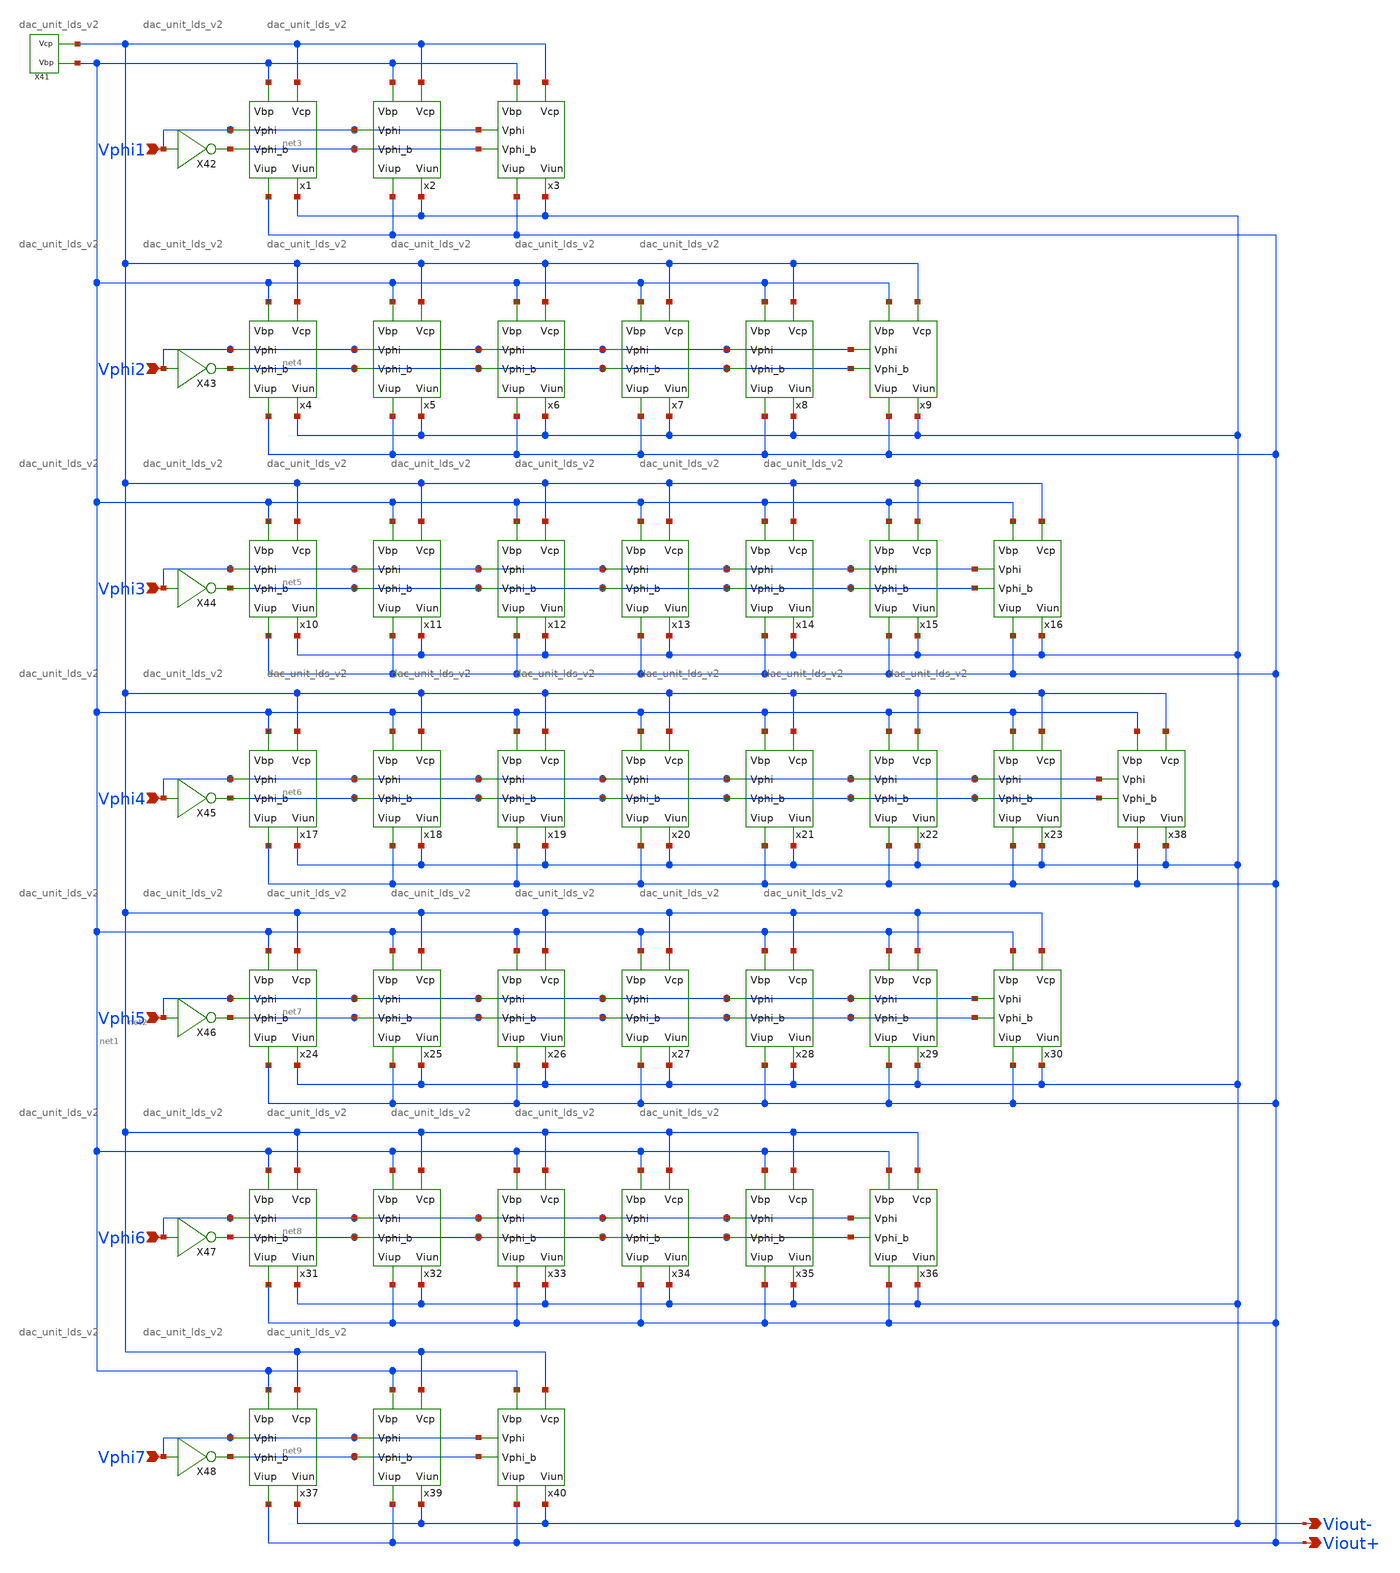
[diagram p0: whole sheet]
** sch_path: simulation/dac_lds.sch
**.subckt dac_lds Vphi1 Vphi2 Vphi3 Vphi4 Vphi5 Vphi6 Vphi7 Viout+ Viout-
*.ipin Vphi1
*.ipin Vphi2
*.ipin Vphi3
*.ipin Vphi4
*.ipin Vphi5
*.ipin Vphi6
*.ipin Vphi7
*.opin Viout+
*.opin Viout-
x1 net1 net2 Viout+ Viout- Vphi1 net3 dac_unit_lds_v2
x2 net1 net2 Viout+ Viout- Vphi1 net3 dac_unit_lds_v2
x3 net1 net2 Viout+ Viout- Vphi1 net3 dac_unit_lds_v2
x4 net1 net2 Viout+ Viout- Vphi2 net4 dac_unit_lds_v2
x5 net1 net2 Viout+ Viout- Vphi2 net4 dac_unit_lds_v2
x6 net1 net2 Viout+ Viout- Vphi2 net4 dac_unit_lds_v2
x7 net1 net2 Viout+ Viout- Vphi2 net4 dac_unit_lds_v2
x8 net1 net2 Viout+ Viout- Vphi2 net4 dac_unit_lds_v2
x9 net1 net2 Viout+ Viout- Vphi2 net4 dac_unit_lds_v2
x10 net1 net2 Viout+ Viout- Vphi3 net5 dac_unit_lds_v2
x11 net1 net2 Viout+ Viout- Vphi3 net5 dac_unit_lds_v2
x12 net1 net2 Viout+ Viout- Vphi3 net5 dac_unit_lds_v2
x13 net1 net2 Viout+ Viout- Vphi3 net5 dac_unit_lds_v2
x14 net1 net2 Viout+ Viout- Vphi3 net5 dac_unit_lds_v2
x15 net1 net2 Viout+ Viout- Vphi3 net5 dac_unit_lds_v2
x16 net1 net2 Viout+ Viout- Vphi3 net5 dac_unit_lds_v2
x17 net1 net2 Viout+ Viout- Vphi4 net6 dac_unit_lds_v2
x18 net1 net2 Viout+ Viout- Vphi4 net6 dac_unit_lds_v2
x19 net1 net2 Viout+ Viout- Vphi4 net6 dac_unit_lds_v2
x20 net1 net2 Viout+ Viout- Vphi4 net6 dac_unit_lds_v2
x21 net1 net2 Viout+ Viout- Vphi4 net6 dac_unit_lds_v2
x22 net1 net2 Viout+ Viout- Vphi4 net6 dac_unit_lds_v2
x23 net1 net2 Viout+ Viout- Vphi4 net6 dac_unit_lds_v2
x24 net1 net2 Viout+ Viout- Vphi5 net7 dac_unit_lds_v2
x25 net1 net2 Viout+ Viout- Vphi5 net7 dac_unit_lds_v2
x26 net1 net2 Viout+ Viout- Vphi5 net7 dac_unit_lds_v2
x27 net1 net2 Viout+ Viout- Vphi5 net7 dac_unit_lds_v2
x28 net1 net2 Viout+ Viout- Vphi5 net7 dac_unit_lds_v2
x29 net1 net2 Viout+ Viout- Vphi5 net7 dac_unit_lds_v2
x30 net1 net2 Viout+ Viout- Vphi5 net7 dac_unit_lds_v2
x31 net1 net2 Viout+ Viout- Vphi6 net8 dac_unit_lds_v2
x32 net1 net2 Viout+ Viout- Vphi6 net8 dac_unit_lds_v2
x33 net1 net2 Viout+ Viout- Vphi6 net8 dac_unit_lds_v2
x34 net1 net2 Viout+ Viout- Vphi6 net8 dac_unit_lds_v2
x35 net1 net2 Viout+ Viout- Vphi6 net8 dac_unit_lds_v2
x36 net1 net2 Viout+ Viout- Vphi6 net8 dac_unit_lds_v2
x38 net1 net2 Viout+ Viout- Vphi4 net6 dac_unit_lds_v2
x37 net1 net2 Viout+ Viout- Vphi7 net9 dac_unit_lds_v2
x39 net1 net2 Viout+ Viout- Vphi7 net9 dac_unit_lds_v2
x40 net1 net2 Viout+ Viout- Vphi7 net9 dac_unit_lds_v2
X41 net2 net1 v_gen_lds
X42 Vphi1 net3 inverter
X43 Vphi2 net4 inverter
X44 Vphi3 net5 inverter
X45 Vphi4 net6 inverter
X46 Vphi5 net7 inverter
X47 Vphi6 net8 inverter
X48 Vphi7 net9 inverter
**.ends

* expanding   symbol:  ./dac/dac_unit_lds_v2.sym # of pins=6
** sym_path: simulation/dac/dac_unit_lds_v2.sym
** sch_path: simulation/dac/dac_unit_lds_v2.sch
.subckt dac_unit_lds_v2 Vbp Vcp Viup Viun Vphi Vphi_b
*.ipin Vphi
*.ipin Vbp
*.ipin Vcp
*.opin Viun
*.opin Viup
*.ipin Vphi_b
XM1 net1 Vbp VDD VDD sky130_fd_pr__pfet_01v8 L=0.5 W=6 nf=1 ad='int((nf+1)/2) * W/nf * 0.29' as='int((nf+2)/2) * W/nf * 0.29'
+ pd='2*int((nf+1)/2) * (W/nf + 0.29)' ps='2*int((nf+2)/2) * (W/nf + 0.29)' nrd='0.29 / W' nrs='0.29 / W'
+ sa=0 sb=0 sd=0 mult=1 m=1
XM2 net2 Vcp net1 VDD sky130_fd_pr__pfet_01v8 L=0.5 W=6 nf=1 ad='int((nf+1)/2) * W/nf * 0.29' as='int((nf+2)/2) * W/nf * 0.29'
+ pd='2*int((nf+1)/2) * (W/nf + 0.29)' ps='2*int((nf+2)/2) * (W/nf + 0.29)' nrd='0.29 / W' nrs='0.29 / W'
+ sa=0 sb=0 sd=0 mult=1 m=1
XM3 Viun Vphi net2 VDD sky130_fd_pr__pfet_01v8 L=0.5 W=6 nf=1 ad='int((nf+1)/2) * W/nf * 0.29' as='int((nf+2)/2) * W/nf * 0.29'
+ pd='2*int((nf+1)/2) * (W/nf + 0.29)' ps='2*int((nf+2)/2) * (W/nf + 0.29)' nrd='0.29 / W' nrs='0.29 / W'
+ sa=0 sb=0 sd=0 mult=1 m=1
XM4 Viup Vphi_b net2 VDD sky130_fd_pr__pfet_01v8 L=0.5 W=6 nf=1 ad='int((nf+1)/2) * W/nf * 0.29' as='int((nf+2)/2) * W/nf * 0.29'
+ pd='2*int((nf+1)/2) * (W/nf + 0.29)' ps='2*int((nf+2)/2) * (W/nf + 0.29)' nrd='0.29 / W' nrs='0.29 / W'
+ sa=0 sb=0 sd=0 mult=1 m=1
XM5 net3 Vbp VDD VDD sky130_fd_pr__pfet_01v8 L=0.5 W=6 nf=1 ad='int((nf+1)/2) * W/nf * 0.29' as='int((nf+2)/2) * W/nf * 0.29'
+ pd='2*int((nf+1)/2) * (W/nf + 0.29)' ps='2*int((nf+2)/2) * (W/nf + 0.29)' nrd='0.29 / W' nrs='0.29 / W'
+ sa=0 sb=0 sd=0 mult=1 m=1
XM6 net4 Vcp net3 VDD sky130_fd_pr__pfet_01v8 L=0.5 W=6 nf=1 ad='int((nf+1)/2) * W/nf * 0.29' as='int((nf+2)/2) * W/nf * 0.29'
+ pd='2*int((nf+1)/2) * (W/nf + 0.29)' ps='2*int((nf+2)/2) * (W/nf + 0.29)' nrd='0.29 / W' nrs='0.29 / W'
+ sa=0 sb=0 sd=0 mult=1 m=1
XM7 Viun Vphi net4 VDD sky130_fd_pr__pfet_01v8 L=0.5 W=6 nf=1 ad='int((nf+1)/2) * W/nf * 0.29' as='int((nf+2)/2) * W/nf * 0.29'
+ pd='2*int((nf+1)/2) * (W/nf + 0.29)' ps='2*int((nf+2)/2) * (W/nf + 0.29)' nrd='0.29 / W' nrs='0.29 / W'
+ sa=0 sb=0 sd=0 mult=1 m=1
XM8 Viup Vphi_b net4 VDD sky130_fd_pr__pfet_01v8 L=0.5 W=6 nf=1 ad='int((nf+1)/2) * W/nf * 0.29' as='int((nf+2)/2) * W/nf * 0.29'
+ pd='2*int((nf+1)/2) * (W/nf + 0.29)' ps='2*int((nf+2)/2) * (W/nf + 0.29)' nrd='0.29 / W' nrs='0.29 / W'
+ sa=0 sb=0 sd=0 mult=1 m=1
XM9 VDD VDD net1 VDD sky130_fd_pr__pfet_01v8 L=0.5 W=6 nf=1 ad='int((nf+1)/2) * W/nf * 0.29' as='int((nf+2)/2) * W/nf * 0.29'
+ pd='2*int((nf+1)/2) * (W/nf + 0.29)' ps='2*int((nf+2)/2) * (W/nf + 0.29)' nrd='0.29 / W' nrs='0.29 / W'
+ sa=0 sb=0 sd=0 mult=1 m=1
XM10 net1 VDD VDD VDD sky130_fd_pr__pfet_01v8 L=0.5 W=6 nf=1 ad='int((nf+1)/2) * W/nf * 0.29' as='int((nf+2)/2) * W/nf * 0.29'
+ pd='2*int((nf+1)/2) * (W/nf + 0.29)' ps='2*int((nf+2)/2) * (W/nf + 0.29)' nrd='0.29 / W' nrs='0.29 / W'
+ sa=0 sb=0 sd=0 mult=1 m=1
XM11 VDD VDD net3 VDD sky130_fd_pr__pfet_01v8 L=0.5 W=6 nf=1 ad='int((nf+1)/2) * W/nf * 0.29' as='int((nf+2)/2) * W/nf * 0.29'
+ pd='2*int((nf+1)/2) * (W/nf + 0.29)' ps='2*int((nf+2)/2) * (W/nf + 0.29)' nrd='0.29 / W' nrs='0.29 / W'
+ sa=0 sb=0 sd=0 mult=1 m=1
XM12 net3 VDD VDD VDD sky130_fd_pr__pfet_01v8 L=0.5 W=6 nf=1 ad='int((nf+1)/2) * W/nf * 0.29' as='int((nf+2)/2) * W/nf * 0.29'
+ pd='2*int((nf+1)/2) * (W/nf + 0.29)' ps='2*int((nf+2)/2) * (W/nf + 0.29)' nrd='0.29 / W' nrs='0.29 / W'
+ sa=0 sb=0 sd=0 mult=1 m=1
.ends


* expanding   symbol:  ./dac/v_gen_lds.sym # of pins=2
** sym_path: simulation/dac/v_gen_lds.sym
** sch_path: simulation/dac/v_gen_lds.sch
.subckt v_gen_lds Vcp Vbp
*.opin Vcp
*.opin Vbp
XM25 net1 Vcp Vcp VDD sky130_fd_pr__pfet_01v8 L=0.5 W=12 nf=1 ad='int((nf+1)/2) * W/nf * 0.29' as='int((nf+2)/2) * W/nf * 0.29'
+ pd='2*int((nf+1)/2) * (W/nf + 0.29)' ps='2*int((nf+2)/2) * (W/nf + 0.29)' nrd='0.29 / W' nrs='0.29 / W'
+ sa=0 sb=0 sd=0 mult=1 m=1
XM26 Vcp net3 GND GND sky130_fd_pr__nfet_01v8 L=0.5 W=12 nf=1 ad='int((nf+1)/2) * W/nf * 0.29' as='int((nf+2)/2) * W/nf * 0.29'
+ pd='2*int((nf+1)/2) * (W/nf + 0.29)' ps='2*int((nf+2)/2) * (W/nf + 0.29)' nrd='0.29 / W' nrs='0.29 / W'
+ sa=0 sb=0 sd=0 mult=1 m=1
XM27 net2 net2 net1 VDD sky130_fd_pr__pfet_01v8 L=0.5 W=12 nf=1 ad='int((nf+1)/2) * W/nf * 0.29' as='int((nf+2)/2) * W/nf * 0.29'
+ pd='2*int((nf+1)/2) * (W/nf + 0.29)' ps='2*int((nf+2)/2) * (W/nf + 0.29)' nrd='0.29 / W' nrs='0.29 / W'
+ sa=0 sb=0 sd=0 mult=1 m=1
XM28 GND net3 net4 GND sky130_fd_pr__nfet_01v8 L=0.5 W=12 nf=1 ad='int((nf+1)/2) * W/nf * 0.29' as='int((nf+2)/2) * W/nf * 0.29'
+ pd='2*int((nf+1)/2) * (W/nf + 0.29)' ps='2*int((nf+2)/2) * (W/nf + 0.29)' nrd='0.29 / W' nrs='0.29 / W'
+ sa=0 sb=0 sd=0 mult=1 m=1
XM41 net1 net2 net2 VDD sky130_fd_pr__pfet_01v8 L=0.5 W=12 nf=1 ad='int((nf+1)/2) * W/nf * 0.29' as='int((nf+2)/2) * W/nf * 0.29'
+ pd='2*int((nf+1)/2) * (W/nf + 0.29)' ps='2*int((nf+2)/2) * (W/nf + 0.29)' nrd='0.29 / W' nrs='0.29 / W'
+ sa=0 sb=0 sd=0 mult=1 m=1
XM42 net4 net3 net5 GND sky130_fd_pr__nfet_01v8 L=0.5 W=12 nf=1 ad='int((nf+1)/2) * W/nf * 0.29' as='int((nf+2)/2) * W/nf * 0.29'
+ pd='2*int((nf+1)/2) * (W/nf + 0.29)' ps='2*int((nf+2)/2) * (W/nf + 0.29)' nrd='0.29 / W' nrs='0.29 / W'
+ sa=0 sb=0 sd=0 mult=1 m=1
XM43 net2 net2 net1 VDD sky130_fd_pr__pfet_01v8 L=0.5 W=12 nf=1 ad='int((nf+1)/2) * W/nf * 0.29' as='int((nf+2)/2) * W/nf * 0.29'
+ pd='2*int((nf+1)/2) * (W/nf + 0.29)' ps='2*int((nf+2)/2) * (W/nf + 0.29)' nrd='0.29 / W' nrs='0.29 / W'
+ sa=0 sb=0 sd=0 mult=1 m=1
XM44 net5 net3 net6 GND sky130_fd_pr__nfet_01v8 L=0.5 W=12 nf=1 ad='int((nf+1)/2) * W/nf * 0.29' as='int((nf+2)/2) * W/nf * 0.29'
+ pd='2*int((nf+1)/2) * (W/nf + 0.29)' ps='2*int((nf+2)/2) * (W/nf + 0.29)' nrd='0.29 / W' nrs='0.29 / W'
+ sa=0 sb=0 sd=0 mult=1 m=1
XM45 net1 net2 net2 VDD sky130_fd_pr__pfet_01v8 L=0.5 W=12 nf=1 ad='int((nf+1)/2) * W/nf * 0.29' as='int((nf+2)/2) * W/nf * 0.29'
+ pd='2*int((nf+1)/2) * (W/nf + 0.29)' ps='2*int((nf+2)/2) * (W/nf + 0.29)' nrd='0.29 / W' nrs='0.29 / W'
+ sa=0 sb=0 sd=0 mult=1 m=1
XM46 net6 net3 net7 GND sky130_fd_pr__nfet_01v8 L=0.5 W=12 nf=1 ad='int((nf+1)/2) * W/nf * 0.29' as='int((nf+2)/2) * W/nf * 0.29'
+ pd='2*int((nf+1)/2) * (W/nf + 0.29)' ps='2*int((nf+2)/2) * (W/nf + 0.29)' nrd='0.29 / W' nrs='0.29 / W'
+ sa=0 sb=0 sd=0 mult=1 m=1
XM47 VDD net2 net1 VDD sky130_fd_pr__pfet_01v8 L=0.5 W=12 nf=1 ad='int((nf+1)/2) * W/nf * 0.29' as='int((nf+2)/2) * W/nf * 0.29'
+ pd='2*int((nf+1)/2) * (W/nf + 0.29)' ps='2*int((nf+2)/2) * (W/nf + 0.29)' nrd='0.29 / W' nrs='0.29 / W'
+ sa=0 sb=0 sd=0 mult=1 m=1
XM48 net7 net3 net2 GND sky130_fd_pr__nfet_01v8 L=0.5 W=12 nf=1 ad='int((nf+1)/2) * W/nf * 0.29' as='int((nf+2)/2) * W/nf * 0.29'
+ pd='2*int((nf+1)/2) * (W/nf + 0.29)' ps='2*int((nf+2)/2) * (W/nf + 0.29)' nrd='0.29 / W' nrs='0.29 / W'
+ sa=0 sb=0 sd=0 mult=1 m=1
XM54 VDD Vbp Vbp VDD sky130_fd_pr__pfet_01v8 L=0.5 W=12 nf=1 ad='int((nf+1)/2) * W/nf * 0.29' as='int((nf+2)/2) * W/nf * 0.29'
+ pd='2*int((nf+1)/2) * (W/nf + 0.29)' ps='2*int((nf+2)/2) * (W/nf + 0.29)' nrd='0.29 / W' nrs='0.29 / W'
+ sa=0 sb=0 sd=0 mult=1 m=1
XM1 Vbp net3 GND GND sky130_fd_pr__nfet_01v8 L=0.5 W=12 nf=1 ad='int((nf+1)/2) * W/nf * 0.29' as='int((nf+2)/2) * W/nf * 0.29'
+ pd='2*int((nf+1)/2) * (W/nf + 0.29)' ps='2*int((nf+2)/2) * (W/nf + 0.29)' nrd='0.29 / W' nrs='0.29 / W'
+ sa=0 sb=0 sd=0 mult=1 m=1
XM2 net3 net3 GND GND sky130_fd_pr__nfet_01v8 L=0.5 W=12 nf=1 ad='int((nf+1)/2) * W/nf * 0.29' as='int((nf+2)/2) * W/nf * 0.29'
+ pd='2*int((nf+1)/2) * (W/nf + 0.29)' ps='2*int((nf+2)/2) * (W/nf + 0.29)' nrd='0.29 / W' nrs='0.29 / W'
+ sa=0 sb=0 sd=0 mult=1 m=1
XM3 Vcp VDD VDD VDD sky130_fd_pr__pfet_01v8 L=0.5 W=12 nf=1 ad='int((nf+1)/2) * W/nf * 0.29' as='int((nf+2)/2) * W/nf * 0.29'
+ pd='2*int((nf+1)/2) * (W/nf + 0.29)' ps='2*int((nf+2)/2) * (W/nf + 0.29)' nrd='0.29 / W' nrs='0.29 / W'
+ sa=0 sb=0 sd=0 mult=1 m=1
XM16 net8 net13 net13 VDD sky130_fd_pr__pfet_01v8 L=0.5 W=12 nf=1 ad='int((nf+1)/2) * W/nf * 0.29' as='int((nf+2)/2) * W/nf * 0.29'
+ pd='2*int((nf+1)/2) * (W/nf + 0.29)' ps='2*int((nf+2)/2) * (W/nf + 0.29)' nrd='0.29 / W' nrs='0.29 / W'
+ sa=0 sb=0 sd=0 mult=1 m=1
XM17 net13 net3 GND GND sky130_fd_pr__nfet_01v8 L=0.5 W=12 nf=1 ad='int((nf+1)/2) * W/nf * 0.29' as='int((nf+2)/2) * W/nf * 0.29'
+ pd='2*int((nf+1)/2) * (W/nf + 0.29)' ps='2*int((nf+2)/2) * (W/nf + 0.29)' nrd='0.29 / W' nrs='0.29 / W'
+ sa=0 sb=0 sd=0 mult=1 m=1
XM18 net2 net2 net8 VDD sky130_fd_pr__pfet_01v8 L=0.5 W=12 nf=1 ad='int((nf+1)/2) * W/nf * 0.29' as='int((nf+2)/2) * W/nf * 0.29'
+ pd='2*int((nf+1)/2) * (W/nf + 0.29)' ps='2*int((nf+2)/2) * (W/nf + 0.29)' nrd='0.29 / W' nrs='0.29 / W'
+ sa=0 sb=0 sd=0 mult=1 m=1
XM19 GND net3 net9 GND sky130_fd_pr__nfet_01v8 L=0.5 W=12 nf=1 ad='int((nf+1)/2) * W/nf * 0.29' as='int((nf+2)/2) * W/nf * 0.29'
+ pd='2*int((nf+1)/2) * (W/nf + 0.29)' ps='2*int((nf+2)/2) * (W/nf + 0.29)' nrd='0.29 / W' nrs='0.29 / W'
+ sa=0 sb=0 sd=0 mult=1 m=1
XM20 net8 net2 net2 VDD sky130_fd_pr__pfet_01v8 L=0.5 W=12 nf=1 ad='int((nf+1)/2) * W/nf * 0.29' as='int((nf+2)/2) * W/nf * 0.29'
+ pd='2*int((nf+1)/2) * (W/nf + 0.29)' ps='2*int((nf+2)/2) * (W/nf + 0.29)' nrd='0.29 / W' nrs='0.29 / W'
+ sa=0 sb=0 sd=0 mult=1 m=1
XM21 net9 net3 net10 GND sky130_fd_pr__nfet_01v8 L=0.5 W=12 nf=1 ad='int((nf+1)/2) * W/nf * 0.29' as='int((nf+2)/2) * W/nf * 0.29'
+ pd='2*int((nf+1)/2) * (W/nf + 0.29)' ps='2*int((nf+2)/2) * (W/nf + 0.29)' nrd='0.29 / W' nrs='0.29 / W'
+ sa=0 sb=0 sd=0 mult=1 m=1
XM22 net2 net2 net8 VDD sky130_fd_pr__pfet_01v8 L=0.5 W=12 nf=1 ad='int((nf+1)/2) * W/nf * 0.29' as='int((nf+2)/2) * W/nf * 0.29'
+ pd='2*int((nf+1)/2) * (W/nf + 0.29)' ps='2*int((nf+2)/2) * (W/nf + 0.29)' nrd='0.29 / W' nrs='0.29 / W'
+ sa=0 sb=0 sd=0 mult=1 m=1
XM23 net10 net3 net11 GND sky130_fd_pr__nfet_01v8 L=0.5 W=12 nf=1 ad='int((nf+1)/2) * W/nf * 0.29' as='int((nf+2)/2) * W/nf * 0.29'
+ pd='2*int((nf+1)/2) * (W/nf + 0.29)' ps='2*int((nf+2)/2) * (W/nf + 0.29)' nrd='0.29 / W' nrs='0.29 / W'
+ sa=0 sb=0 sd=0 mult=1 m=1
XM24 net8 net2 net2 VDD sky130_fd_pr__pfet_01v8 L=0.5 W=12 nf=1 ad='int((nf+1)/2) * W/nf * 0.29' as='int((nf+2)/2) * W/nf * 0.29'
+ pd='2*int((nf+1)/2) * (W/nf + 0.29)' ps='2*int((nf+2)/2) * (W/nf + 0.29)' nrd='0.29 / W' nrs='0.29 / W'
+ sa=0 sb=0 sd=0 mult=1 m=1
XM49 net11 net3 net12 GND sky130_fd_pr__nfet_01v8 L=0.5 W=12 nf=1 ad='int((nf+1)/2) * W/nf * 0.29' as='int((nf+2)/2) * W/nf * 0.29'
+ pd='2*int((nf+1)/2) * (W/nf + 0.29)' ps='2*int((nf+2)/2) * (W/nf + 0.29)' nrd='0.29 / W' nrs='0.29 / W'
+ sa=0 sb=0 sd=0 mult=1 m=1
XM50 VDD net2 net8 VDD sky130_fd_pr__pfet_01v8 L=0.5 W=12 nf=1 ad='int((nf+1)/2) * W/nf * 0.29' as='int((nf+2)/2) * W/nf * 0.29'
+ pd='2*int((nf+1)/2) * (W/nf + 0.29)' ps='2*int((nf+2)/2) * (W/nf + 0.29)' nrd='0.29 / W' nrs='0.29 / W'
+ sa=0 sb=0 sd=0 mult=1 m=1
XM51 net12 net3 net2 GND sky130_fd_pr__nfet_01v8 L=0.5 W=12 nf=1 ad='int((nf+1)/2) * W/nf * 0.29' as='int((nf+2)/2) * W/nf * 0.29'
+ pd='2*int((nf+1)/2) * (W/nf + 0.29)' ps='2*int((nf+2)/2) * (W/nf + 0.29)' nrd='0.29 / W' nrs='0.29 / W'
+ sa=0 sb=0 sd=0 mult=1 m=1
XM52 VDD Vbp Vbp VDD sky130_fd_pr__pfet_01v8 L=0.5 W=12 nf=1 ad='int((nf+1)/2) * W/nf * 0.29' as='int((nf+2)/2) * W/nf * 0.29'
+ pd='2*int((nf+1)/2) * (W/nf + 0.29)' ps='2*int((nf+2)/2) * (W/nf + 0.29)' nrd='0.29 / W' nrs='0.29 / W'
+ sa=0 sb=0 sd=0 mult=1 m=1
XM53 GND net3 Vbp GND sky130_fd_pr__nfet_01v8 L=0.5 W=12 nf=1 ad='int((nf+1)/2) * W/nf * 0.29' as='int((nf+2)/2) * W/nf * 0.29'
+ pd='2*int((nf+1)/2) * (W/nf + 0.29)' ps='2*int((nf+2)/2) * (W/nf + 0.29)' nrd='0.29 / W' nrs='0.29 / W'
+ sa=0 sb=0 sd=0 mult=1 m=1
XM55 net3 net3 GND GND sky130_fd_pr__nfet_01v8 L=0.5 W=12 nf=1 ad='int((nf+1)/2) * W/nf * 0.29' as='int((nf+2)/2) * W/nf * 0.29'
+ pd='2*int((nf+1)/2) * (W/nf + 0.29)' ps='2*int((nf+2)/2) * (W/nf + 0.29)' nrd='0.29 / W' nrs='0.29 / W'
+ sa=0 sb=0 sd=0 mult=1 m=1
XM56 net13 VDD VDD VDD sky130_fd_pr__pfet_01v8 L=0.5 W=12 nf=1 ad='int((nf+1)/2) * W/nf * 0.29' as='int((nf+2)/2) * W/nf * 0.29'
+ pd='2*int((nf+1)/2) * (W/nf + 0.29)' ps='2*int((nf+2)/2) * (W/nf + 0.29)' nrd='0.29 / W' nrs='0.29 / W'
+ sa=0 sb=0 sd=0 mult=1 m=1
Ib GND net3 2u
.ends


* expanding   symbol:  ./dac/inverter.sym # of pins=2
** sym_path: simulation/dac/inverter.sym
** sch_path: simulation/dac/inverter.sch
.subckt inverter A Y
*.ipin A
*.opin Y
XM1 Y A VDD VDD sky130_fd_pr__pfet_01v8 L=0.15 W=1 nf=1 ad='int((nf+1)/2) * W/nf * 0.29' as='int((nf+2)/2) * W/nf * 0.29'
+ pd='2*int((nf+1)/2) * (W/nf + 0.29)' ps='2*int((nf+2)/2) * (W/nf + 0.29)' nrd='0.29 / W' nrs='0.29 / W'
+ sa=0 sb=0 sd=0 mult=1 m=1
XM2 Y A GND GND sky130_fd_pr__nfet_01v8 L=0.15 W=1 nf=1 ad='int((nf+1)/2) * W/nf * 0.29' as='int((nf+2)/2) * W/nf * 0.29'
+ pd='2*int((nf+1)/2) * (W/nf + 0.29)' ps='2*int((nf+2)/2) * (W/nf + 0.29)' nrd='0.29 / W' nrs='0.29 / W'
+ sa=0 sb=0 sd=0 mult=1 m=1
.ends

.GLOBAL VDD
.GLOBAL GND
.end
